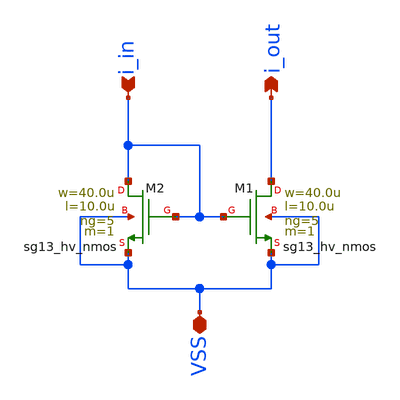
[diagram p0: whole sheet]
** sch_path: macros/heichips26_vcr/macros/switched_capacitor/schematic/xschem/nmos_current_mirror1.sch
**.subckt nmos_current_mirror1 i_in i_out VSS
*.ipin i_in
*.opin i_out
*.iopin VSS
XM1 i_out i_in VSS VSS sg13_hv_nmos w=40.0u l=10.0u ng=5 m=1 mm_ok=1
XM2 i_in i_in VSS VSS sg13_hv_nmos w=40.0u l=10.0u ng=5 m=1 mm_ok=1
**.ends
.end
